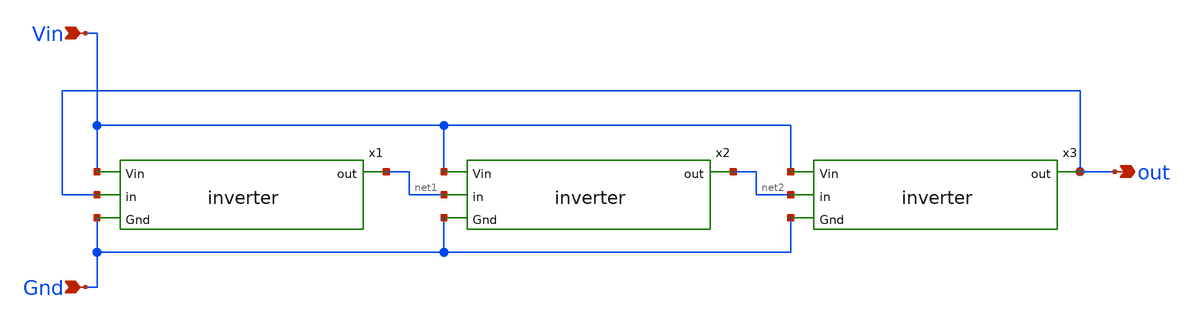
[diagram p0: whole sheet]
** sch_path: Inverter-Ringoscillator/Ringoscillator.sch
**.subckt Ringoscillator out Vin Gnd
*.opin out
*.ipin Vin
*.ipin Gnd
x1 Vin out net1 Gnd inverter
x2 Vin net1 net2 Gnd inverter
x3 Vin net2 out Gnd inverter
**.ends

* expanding   symbol:  inverter.sym # of pins=4
** sym_path: Inverter-Ringoscillator/inverter.sym
** sch_path: Inverter-Ringoscillator/inverter.sch
.subckt inverter Vin in out Gnd
*.ipin in
*.ipin Vin
*.ipin Gnd
*.opin out
XM1 out in Gnd Gnd sky130_fd_pr__nfet_01v8 L=0.15 W=1 nf=1 ad='int((nf+1)/2) * W/nf * 0.29' as='int((nf+2)/2) * W/nf * 0.29'
+ pd='2*int((nf+1)/2) * (W/nf + 0.29)' ps='2*int((nf+2)/2) * (W/nf + 0.29)' nrd='0.29 / W' nrs='0.29 / W'
+ sa=0 sb=0 sd=0 mult=1 m=1
XM2 out in Vin Vin sky130_fd_pr__pfet_01v8 L=0.15 W=1 nf=1 ad='int((nf+1)/2) * W/nf * 0.29' as='int((nf+2)/2) * W/nf * 0.29'
+ pd='2*int((nf+1)/2) * (W/nf + 0.29)' ps='2*int((nf+2)/2) * (W/nf + 0.29)' nrd='0.29 / W' nrs='0.29 / W'
+ sa=0 sb=0 sd=0 mult=1 m=1
.ends

.end
